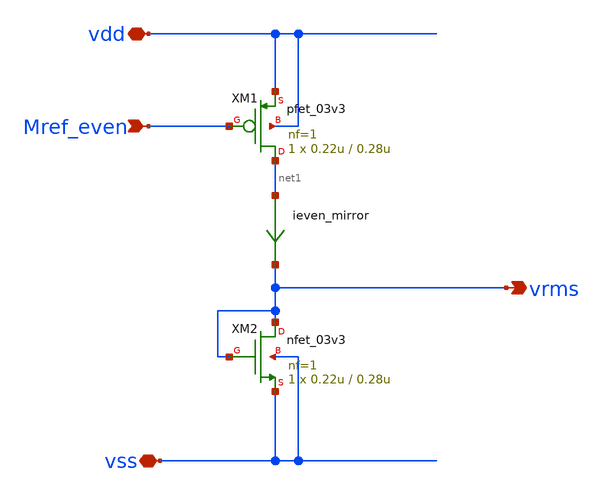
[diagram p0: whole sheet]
** sch_path: designs/libs/core_analog/rms_out/rms_out.sch
**.subckt rms_out Mref_even vdd vss vrms
*.ipin Mref_even
*.iopin vdd
*.iopin vss
*.opin vrms
XM1 net1 Mref_even vdd vdd pfet_03v3 L=0.28u W=0.22u nf=1 ad='int((nf+1)/2) * W/nf * 0.18u' as='int((nf+2)/2) * W/nf * 0.18u'
+ pd='2*int((nf+1)/2) * (W/nf + 0.18u)' ps='2*int((nf+2)/2) * (W/nf + 0.18u)' nrd='0.18u / W' nrs='0.18u / W'
+ sa=0 sb=0 sd=0 m=1
ieven_mirror net1 vrms 0
.save i(ieven_mirror)
XM2 vrms vrms vss vss nfet_03v3 L=0.28u W=0.22u nf=1 ad='int((nf+1)/2) * W/nf * 0.18u' as='int((nf+2)/2) * W/nf * 0.18u'
+ pd='2*int((nf+1)/2) * (W/nf + 0.18u)' ps='2*int((nf+2)/2) * (W/nf + 0.18u)' nrd='0.18u / W' nrs='0.18u / W'
+ sa=0 sb=0 sd=0 m=1
**.ends
.end
